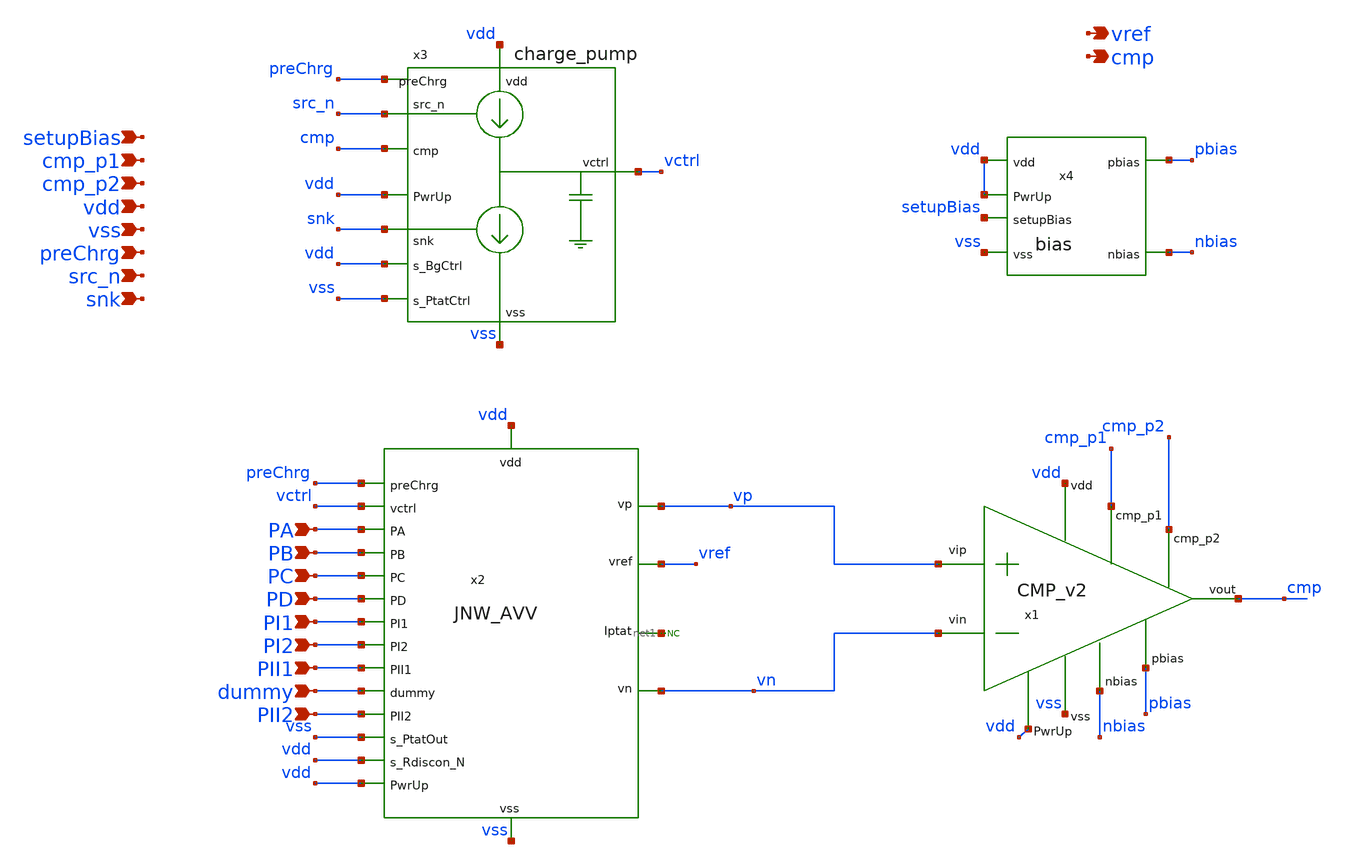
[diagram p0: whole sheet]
** sch_path: design/JNW_AVV_SKY130A/TB_Vref.sch
**.subckt TB_Vref vdd vss src_n snk PA PB PC PD PI1 PI2 PII1 preChrg dummy PII2 setupBias cmp_p1
*+ cmp_p2 vref cmp
*.ipin vdd
*.ipin vss
*.ipin src_n
*.ipin snk
*.ipin PA
*.ipin PB
*.ipin PC
*.ipin PD
*.ipin PI1
*.ipin PI2
*.ipin PII1
*.ipin preChrg
*.ipin dummy
*.ipin PII2
*.ipin setupBias
*.ipin cmp_p1
*.ipin cmp_p2
*.opin vref
*.opin cmp
x1 vdd pbias cmp vn vp vss cmp_p1 cmp_p2 nbias vdd CMP_v2
x2 vctrl PA PD vref vdd vss PC PB dummy PI2 PI1 PII1 vn vp PII2 preChrg net1 vss vdd vdd JNW_AVV
x4 pbias vdd nbias vss setupBias vdd bias
x3 vdd cmp src_n vctrl snk vss preChrg vdd vss vdd charge_pump
* noconn #net1
**.ends
.end
